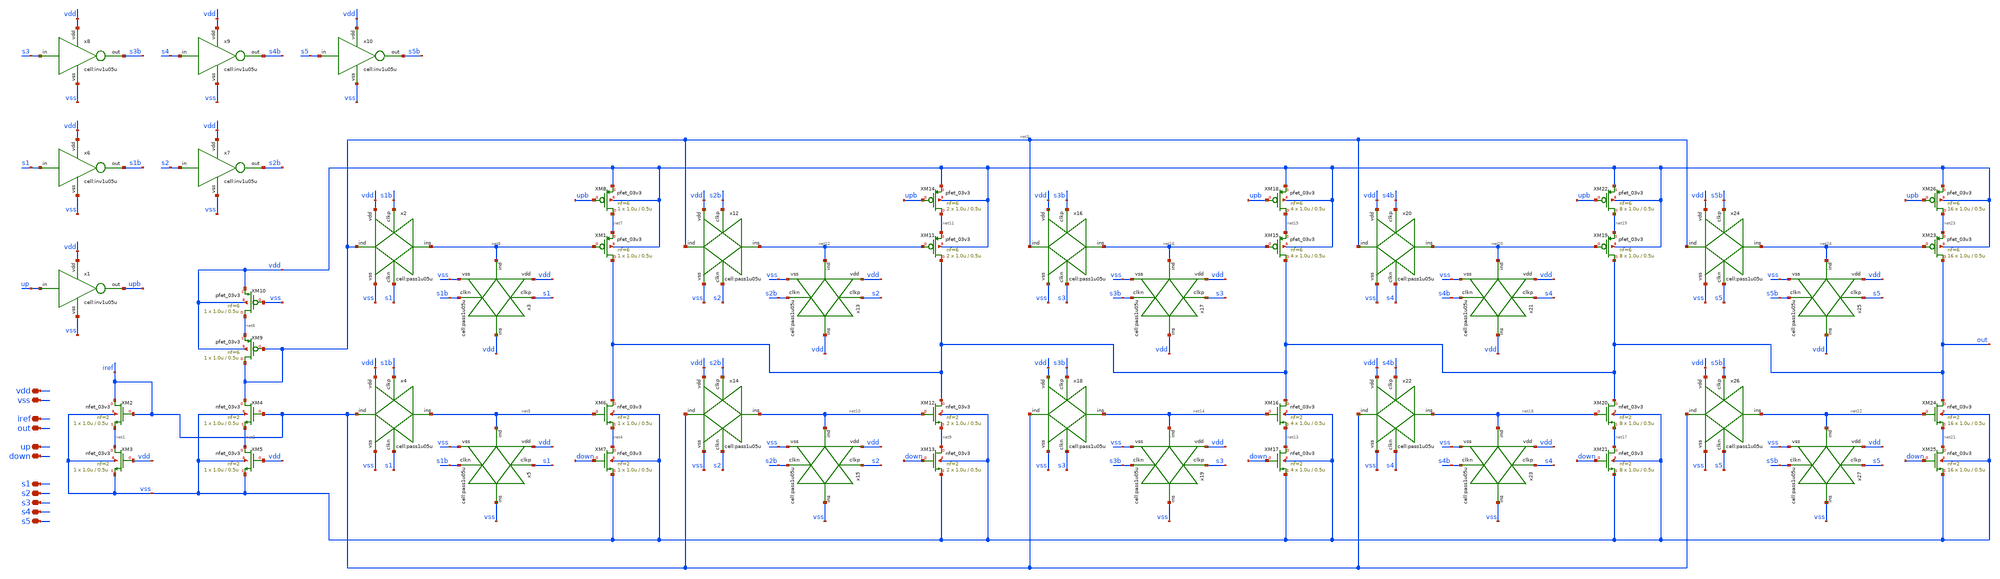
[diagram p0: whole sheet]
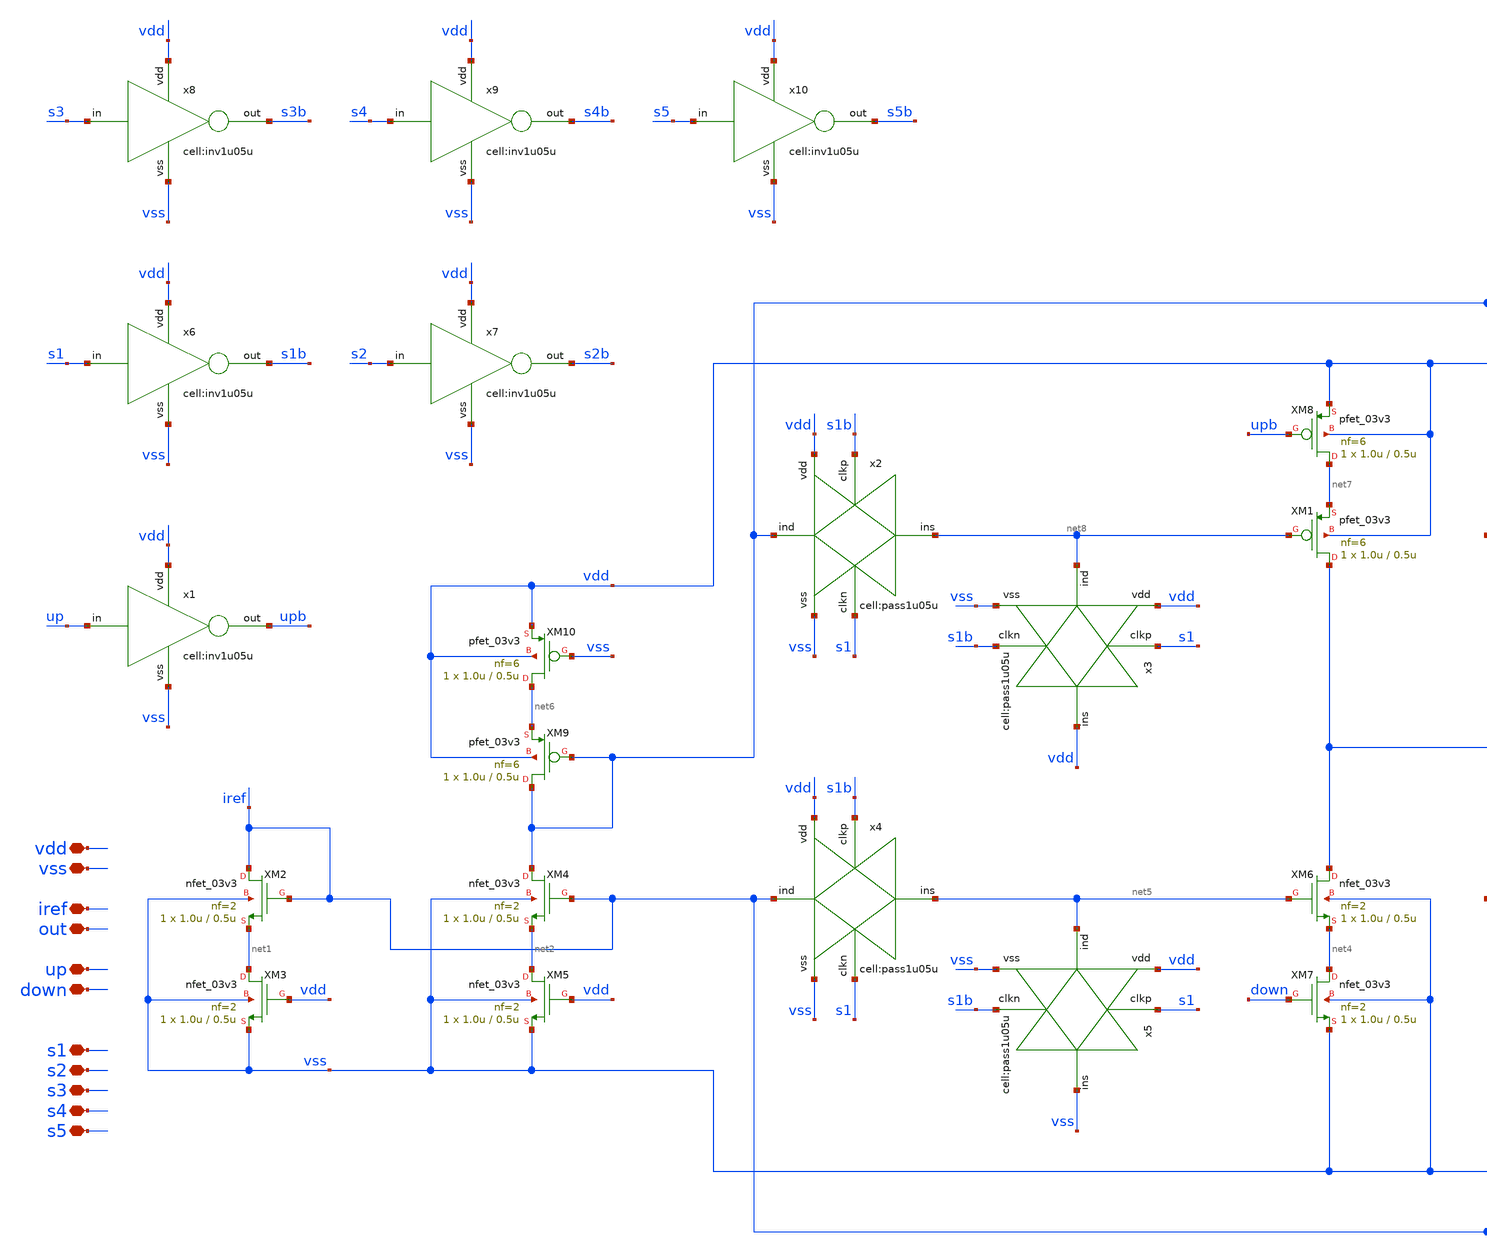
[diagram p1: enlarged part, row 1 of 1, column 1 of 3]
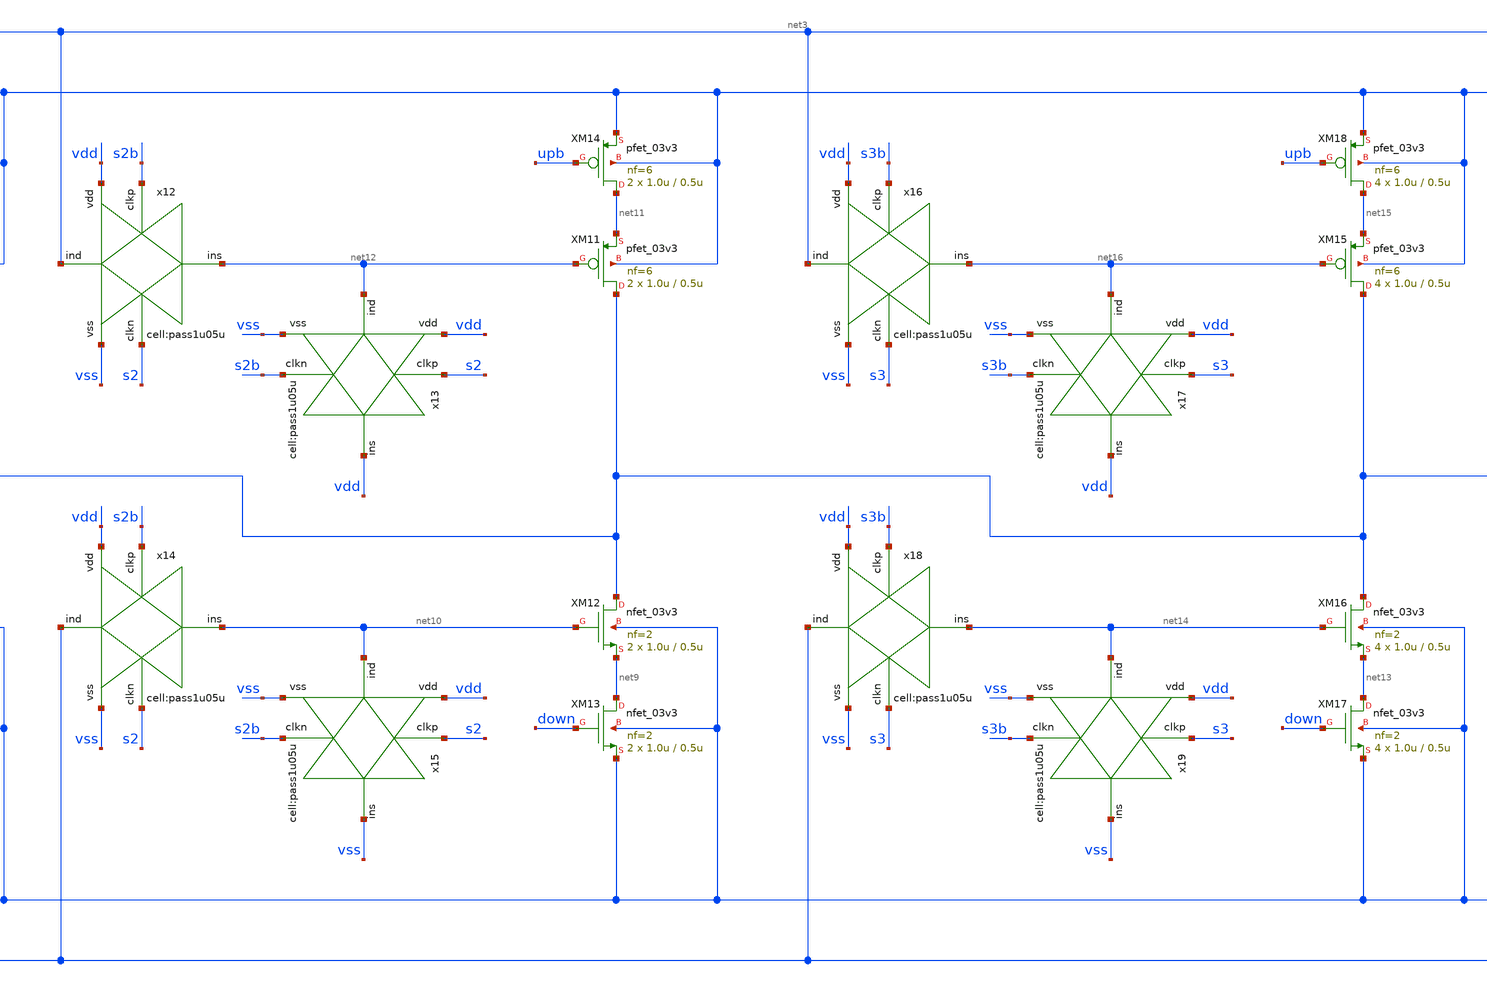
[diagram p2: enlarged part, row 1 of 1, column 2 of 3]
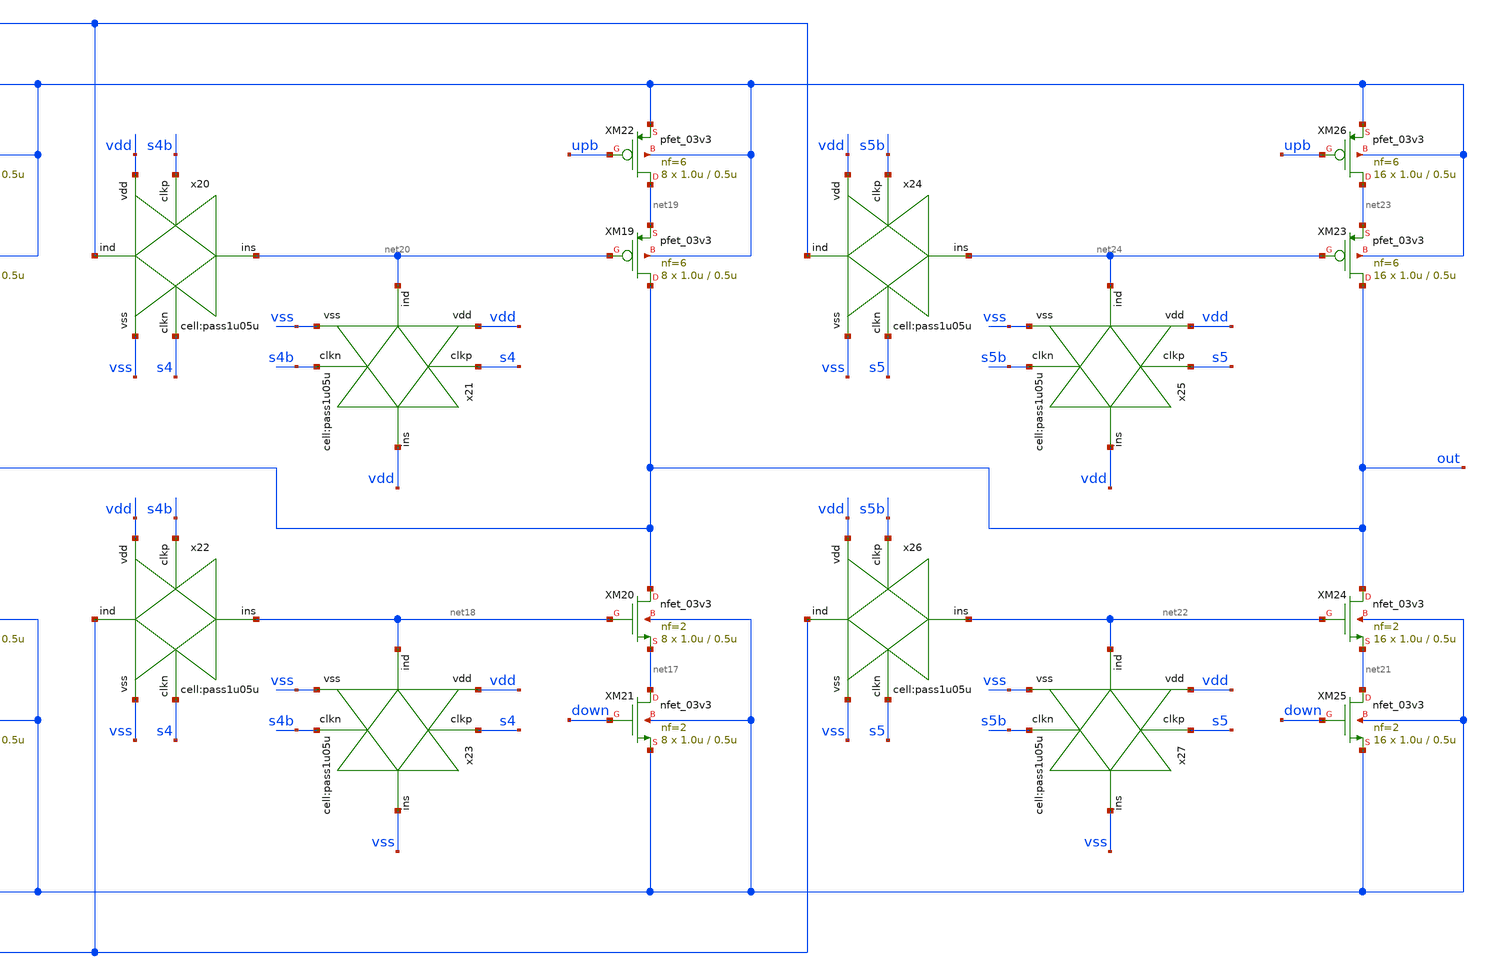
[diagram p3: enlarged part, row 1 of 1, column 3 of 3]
** sch_path: designs/libs/core_analog/asc_programmable_basic_pump/asc_programmable_basic_pump.sch
**.subckt asc_programmable_basic_pump vdd vss up down iref out s3 s4 s1 s2 s5
*.iopin vdd
*.iopin vss
*.iopin up
*.iopin down
*.iopin iref
*.iopin out
*.iopin s3
*.iopin s4
*.iopin s1
*.iopin s2
*.iopin s5
XM1 out net8 net7 vdd pfet_03v3 L=0.5u W=1.0u nf=6 ad='int((nf+1)/2) * W/nf * 0.18u' as='int((nf+2)/2) * W/nf * 0.18u'
+ pd='2*int((nf+1)/2) * (W/nf + 0.18u)' ps='2*int((nf+2)/2) * (W/nf + 0.18u)' nrd='0.18u / W' nrs='0.18u / W'
+ sa=0 sb=0 sd=0 m=1
XM2 iref iref net1 vss nfet_03v3 L=0.5u W=1.0u nf=2 ad='int((nf+1)/2) * W/nf * 0.18u' as='int((nf+2)/2) * W/nf * 0.18u'
+ pd='2*int((nf+1)/2) * (W/nf + 0.18u)' ps='2*int((nf+2)/2) * (W/nf + 0.18u)' nrd='0.18u / W' nrs='0.18u / W'
+ sa=0 sb=0 sd=0 m=1
XM3 net1 vdd vss vss nfet_03v3 L=0.5u W=1.0u nf=2 ad='int((nf+1)/2) * W/nf * 0.18u' as='int((nf+2)/2) * W/nf * 0.18u'
+ pd='2*int((nf+1)/2) * (W/nf + 0.18u)' ps='2*int((nf+2)/2) * (W/nf + 0.18u)' nrd='0.18u / W' nrs='0.18u / W'
+ sa=0 sb=0 sd=0 m=1
XM4 net3 iref net2 vss nfet_03v3 L=0.5u W=1.0u nf=2 ad='int((nf+1)/2) * W/nf * 0.18u' as='int((nf+2)/2) * W/nf * 0.18u'
+ pd='2*int((nf+1)/2) * (W/nf + 0.18u)' ps='2*int((nf+2)/2) * (W/nf + 0.18u)' nrd='0.18u / W' nrs='0.18u / W'
+ sa=0 sb=0 sd=0 m=1
XM5 net2 vdd vss vss nfet_03v3 L=0.5u W=1.0u nf=2 ad='int((nf+1)/2) * W/nf * 0.18u' as='int((nf+2)/2) * W/nf * 0.18u'
+ pd='2*int((nf+1)/2) * (W/nf + 0.18u)' ps='2*int((nf+2)/2) * (W/nf + 0.18u)' nrd='0.18u / W' nrs='0.18u / W'
+ sa=0 sb=0 sd=0 m=1
XM6 out net5 net4 vss nfet_03v3 L=0.5u W=1.0u nf=2 ad='int((nf+1)/2) * W/nf * 0.18u' as='int((nf+2)/2) * W/nf * 0.18u'
+ pd='2*int((nf+1)/2) * (W/nf + 0.18u)' ps='2*int((nf+2)/2) * (W/nf + 0.18u)' nrd='0.18u / W' nrs='0.18u / W'
+ sa=0 sb=0 sd=0 m=1
XM7 net4 down vss vss nfet_03v3 L=0.5u W=1.0u nf=2 ad='int((nf+1)/2) * W/nf * 0.18u' as='int((nf+2)/2) * W/nf * 0.18u'
+ pd='2*int((nf+1)/2) * (W/nf + 0.18u)' ps='2*int((nf+2)/2) * (W/nf + 0.18u)' nrd='0.18u / W' nrs='0.18u / W'
+ sa=0 sb=0 sd=0 m=1
XM8 net7 upb vdd vdd pfet_03v3 L=0.5u W=1.0u nf=6 ad='int((nf+1)/2) * W/nf * 0.18u' as='int((nf+2)/2) * W/nf * 0.18u'
+ pd='2*int((nf+1)/2) * (W/nf + 0.18u)' ps='2*int((nf+2)/2) * (W/nf + 0.18u)' nrd='0.18u / W' nrs='0.18u / W'
+ sa=0 sb=0 sd=0 m=1
XM9 net3 net3 net6 vdd pfet_03v3 L=0.5u W=1.0u nf=6 ad='int((nf+1)/2) * W/nf * 0.18u' as='int((nf+2)/2) * W/nf * 0.18u'
+ pd='2*int((nf+1)/2) * (W/nf + 0.18u)' ps='2*int((nf+2)/2) * (W/nf + 0.18u)' nrd='0.18u / W' nrs='0.18u / W'
+ sa=0 sb=0 sd=0 m=1
XM10 net6 vss vdd vdd pfet_03v3 L=0.5u W=1.0u nf=6 ad='int((nf+1)/2) * W/nf * 0.18u' as='int((nf+2)/2) * W/nf * 0.18u'
+ pd='2*int((nf+1)/2) * (W/nf + 0.18u)' ps='2*int((nf+2)/2) * (W/nf + 0.18u)' nrd='0.18u / W' nrs='0.18u / W'
+ sa=0 sb=0 sd=0 m=1
x1 up vdd upb vss inv1u05u
x2 net3 vss s1 net8 s1b vdd pass1u05u
x3 net8 vss s1b vdd s1 vdd pass1u05u
x4 iref vss s1 net5 s1b vdd pass1u05u
x5 net5 vss s1b vss s1 vdd pass1u05u
x6 s1 vdd s1b vss inv1u05u
x7 s2 vdd s2b vss inv1u05u
x8 s3 vdd s3b vss inv1u05u
x9 s4 vdd s4b vss inv1u05u
x10 s5 vdd s5b vss inv1u05u
XM11 out net12 net11 vdd pfet_03v3 L=0.5u W=1.0u nf=6 ad='int((nf+1)/2) * W/nf * 0.18u' as='int((nf+2)/2) * W/nf * 0.18u'
+ pd='2*int((nf+1)/2) * (W/nf + 0.18u)' ps='2*int((nf+2)/2) * (W/nf + 0.18u)' nrd='0.18u / W' nrs='0.18u / W'
+ sa=0 sb=0 sd=0 m=2
XM12 out net10 net9 vss nfet_03v3 L=0.5u W=1.0u nf=2 ad='int((nf+1)/2) * W/nf * 0.18u' as='int((nf+2)/2) * W/nf * 0.18u'
+ pd='2*int((nf+1)/2) * (W/nf + 0.18u)' ps='2*int((nf+2)/2) * (W/nf + 0.18u)' nrd='0.18u / W' nrs='0.18u / W'
+ sa=0 sb=0 sd=0 m=2
XM13 net9 down vss vss nfet_03v3 L=0.5u W=1.0u nf=2 ad='int((nf+1)/2) * W/nf * 0.18u' as='int((nf+2)/2) * W/nf * 0.18u'
+ pd='2*int((nf+1)/2) * (W/nf + 0.18u)' ps='2*int((nf+2)/2) * (W/nf + 0.18u)' nrd='0.18u / W' nrs='0.18u / W'
+ sa=0 sb=0 sd=0 m=2
XM14 net11 upb vdd vdd pfet_03v3 L=0.5u W=1.0u nf=6 ad='int((nf+1)/2) * W/nf * 0.18u' as='int((nf+2)/2) * W/nf * 0.18u'
+ pd='2*int((nf+1)/2) * (W/nf + 0.18u)' ps='2*int((nf+2)/2) * (W/nf + 0.18u)' nrd='0.18u / W' nrs='0.18u / W'
+ sa=0 sb=0 sd=0 m=2
x12 net3 vss s2 net12 s2b vdd pass1u05u
x13 net12 vss s2b vdd s2 vdd pass1u05u
x14 iref vss s2 net10 s2b vdd pass1u05u
x15 net10 vss s2b vss s2 vdd pass1u05u
XM15 out net16 net15 vdd pfet_03v3 L=0.5u W=1.0u nf=6 ad='int((nf+1)/2) * W/nf * 0.18u' as='int((nf+2)/2) * W/nf * 0.18u'
+ pd='2*int((nf+1)/2) * (W/nf + 0.18u)' ps='2*int((nf+2)/2) * (W/nf + 0.18u)' nrd='0.18u / W' nrs='0.18u / W'
+ sa=0 sb=0 sd=0 m=4
XM16 out net14 net13 vss nfet_03v3 L=0.5u W=1.0u nf=2 ad='int((nf+1)/2) * W/nf * 0.18u' as='int((nf+2)/2) * W/nf * 0.18u'
+ pd='2*int((nf+1)/2) * (W/nf + 0.18u)' ps='2*int((nf+2)/2) * (W/nf + 0.18u)' nrd='0.18u / W' nrs='0.18u / W'
+ sa=0 sb=0 sd=0 m=4
XM17 net13 down vss vss nfet_03v3 L=0.5u W=1.0u nf=2 ad='int((nf+1)/2) * W/nf * 0.18u' as='int((nf+2)/2) * W/nf * 0.18u'
+ pd='2*int((nf+1)/2) * (W/nf + 0.18u)' ps='2*int((nf+2)/2) * (W/nf + 0.18u)' nrd='0.18u / W' nrs='0.18u / W'
+ sa=0 sb=0 sd=0 m=4
XM18 net15 upb vdd vdd pfet_03v3 L=0.5u W=1.0u nf=6 ad='int((nf+1)/2) * W/nf * 0.18u' as='int((nf+2)/2) * W/nf * 0.18u'
+ pd='2*int((nf+1)/2) * (W/nf + 0.18u)' ps='2*int((nf+2)/2) * (W/nf + 0.18u)' nrd='0.18u / W' nrs='0.18u / W'
+ sa=0 sb=0 sd=0 m=4
x16 net3 vss s3 net16 s3b vdd pass1u05u
x17 net16 vss s3b vdd s3 vdd pass1u05u
x18 iref vss s3 net14 s3b vdd pass1u05u
x19 net14 vss s3b vss s3 vdd pass1u05u
XM19 out net20 net19 vdd pfet_03v3 L=0.5u W=1.0u nf=6 ad='int((nf+1)/2) * W/nf * 0.18u' as='int((nf+2)/2) * W/nf * 0.18u'
+ pd='2*int((nf+1)/2) * (W/nf + 0.18u)' ps='2*int((nf+2)/2) * (W/nf + 0.18u)' nrd='0.18u / W' nrs='0.18u / W'
+ sa=0 sb=0 sd=0 m=8
XM20 out net18 net17 vss nfet_03v3 L=0.5u W=1.0u nf=2 ad='int((nf+1)/2) * W/nf * 0.18u' as='int((nf+2)/2) * W/nf * 0.18u'
+ pd='2*int((nf+1)/2) * (W/nf + 0.18u)' ps='2*int((nf+2)/2) * (W/nf + 0.18u)' nrd='0.18u / W' nrs='0.18u / W'
+ sa=0 sb=0 sd=0 m=8
XM21 net17 down vss vss nfet_03v3 L=0.5u W=1.0u nf=2 ad='int((nf+1)/2) * W/nf * 0.18u' as='int((nf+2)/2) * W/nf * 0.18u'
+ pd='2*int((nf+1)/2) * (W/nf + 0.18u)' ps='2*int((nf+2)/2) * (W/nf + 0.18u)' nrd='0.18u / W' nrs='0.18u / W'
+ sa=0 sb=0 sd=0 m=8
XM22 net19 upb vdd vdd pfet_03v3 L=0.5u W=1.0u nf=6 ad='int((nf+1)/2) * W/nf * 0.18u' as='int((nf+2)/2) * W/nf * 0.18u'
+ pd='2*int((nf+1)/2) * (W/nf + 0.18u)' ps='2*int((nf+2)/2) * (W/nf + 0.18u)' nrd='0.18u / W' nrs='0.18u / W'
+ sa=0 sb=0 sd=0 m=8
x20 net3 vss s4 net20 s4b vdd pass1u05u
x21 net20 vss s4b vdd s4 vdd pass1u05u
x22 iref vss s4 net18 s4b vdd pass1u05u
x23 net18 vss s4b vss s4 vdd pass1u05u
XM23 out net24 net23 vdd pfet_03v3 L=0.5u W=1.0u nf=6 ad='int((nf+1)/2) * W/nf * 0.18u' as='int((nf+2)/2) * W/nf * 0.18u'
+ pd='2*int((nf+1)/2) * (W/nf + 0.18u)' ps='2*int((nf+2)/2) * (W/nf + 0.18u)' nrd='0.18u / W' nrs='0.18u / W'
+ sa=0 sb=0 sd=0 m=16
XM24 out net22 net21 vss nfet_03v3 L=0.5u W=1.0u nf=2 ad='int((nf+1)/2) * W/nf * 0.18u' as='int((nf+2)/2) * W/nf * 0.18u'
+ pd='2*int((nf+1)/2) * (W/nf + 0.18u)' ps='2*int((nf+2)/2) * (W/nf + 0.18u)' nrd='0.18u / W' nrs='0.18u / W'
+ sa=0 sb=0 sd=0 m=16
XM25 net21 down vss vss nfet_03v3 L=0.5u W=1.0u nf=2 ad='int((nf+1)/2) * W/nf * 0.18u' as='int((nf+2)/2) * W/nf * 0.18u'
+ pd='2*int((nf+1)/2) * (W/nf + 0.18u)' ps='2*int((nf+2)/2) * (W/nf + 0.18u)' nrd='0.18u / W' nrs='0.18u / W'
+ sa=0 sb=0 sd=0 m=16
XM26 net23 upb vdd vdd pfet_03v3 L=0.5u W=1.0u nf=6 ad='int((nf+1)/2) * W/nf * 0.18u' as='int((nf+2)/2) * W/nf * 0.18u'
+ pd='2*int((nf+1)/2) * (W/nf + 0.18u)' ps='2*int((nf+2)/2) * (W/nf + 0.18u)' nrd='0.18u / W' nrs='0.18u / W'
+ sa=0 sb=0 sd=0 m=16
x24 net3 vss s5 net24 s5b vdd pass1u05u
x25 net24 vss s5b vdd s5 vdd pass1u05u
x26 iref vss s5 net22 s5b vdd pass1u05u
x27 net22 vss s5b vss s5 vdd pass1u05u
**.ends
.end
